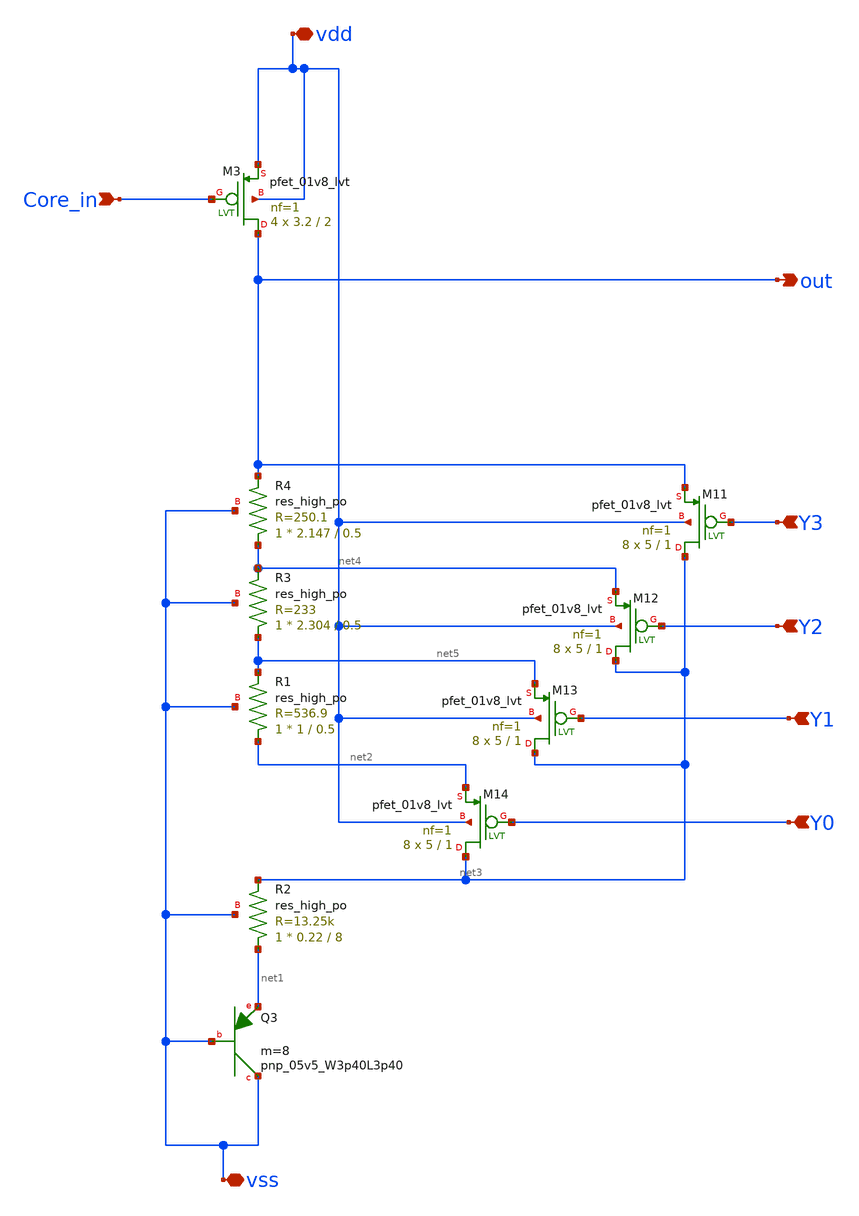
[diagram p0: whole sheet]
** sch_path: Vref_mirror.sch
**.subckt Vref_mirror out vdd vss Core_in Y3 Y2 Y1 Y0
*.opin out
*.iopin vdd
*.iopin vss
*.ipin Core_in
*.ipin Y3
*.ipin Y2
*.ipin Y1
*.ipin Y0
XM3 out Core_in vdd vdd sky130_fd_pr__pfet_01v8_lvt L=2 W=3.2 nf=1 ad='int((1 + 1)/2) * 3.2 / 1 * 0.29'
+ as='int((1 + 2)/2) * 3.2 / 1 * 0.29' pd='2*int((1 + 1)/2) * (3.2 / 1 + 0.29)' ps='2*int((1 + 2)/2) * (3.2 / 1 + 0.29)'
+ nrd='0.29 / 3.2 ' nrs='0.29 / 3.2 ' sa=0 sb=0 sd=0 mult=4 m=4
XQ3 vss vss net1 sky130_fd_pr__pnp_05v5_W3p40L3p40 m=8
XR2 net1 net3 vss sky130_fd_pr__res_high_po W=0.22 L=8 mult=1 m=1
XM11 net3 Y3 out vdd sky130_fd_pr__pfet_01v8_lvt L=1 W=5 nf=1 ad='int((1 + 1)/2) * 5 / 1 * 0.29' as='int((1 + 2)/2) * 5 / 1 * 0.29'
+ pd='2*int((1 + 1)/2) * (5 / 1 + 0.29)' ps='2*int((1 + 2)/2) * (5 / 1 + 0.29)' nrd='0.29 / 5 ' nrs='0.29 / 5 '
+ sa=0 sb=0 sd=0 mult=8 m=8
XM12 net3 Y2 net4 vdd sky130_fd_pr__pfet_01v8_lvt L=1 W=5 nf=1 ad='int((1 + 1)/2) * 5 / 1 * 0.29' as='int((1 + 2)/2) * 5 / 1 * 0.29'
+ pd='2*int((1 + 1)/2) * (5 / 1 + 0.29)' ps='2*int((1 + 2)/2) * (5 / 1 + 0.29)' nrd='0.29 / 5 ' nrs='0.29 / 5 '
+ sa=0 sb=0 sd=0 mult=8 m=8
XM13 net3 Y1 net5 vdd sky130_fd_pr__pfet_01v8_lvt L=1 W=5 nf=1 ad='int((1 + 1)/2) * 5 / 1 * 0.29' as='int((1 + 2)/2) * 5 / 1 * 0.29'
+ pd='2*int((1 + 1)/2) * (5 / 1 + 0.29)' ps='2*int((1 + 2)/2) * (5 / 1 + 0.29)' nrd='0.29 / 5 ' nrs='0.29 / 5 '
+ sa=0 sb=0 sd=0 mult=8 m=8
XM14 net3 Y0 net2 vdd sky130_fd_pr__pfet_01v8_lvt L=1 W=5 nf=1 ad='int((1 + 1)/2) * 5 / 1 * 0.29' as='int((1 + 2)/2) * 5 / 1 * 0.29'
+ pd='2*int((1 + 1)/2) * (5 / 1 + 0.29)' ps='2*int((1 + 2)/2) * (5 / 1 + 0.29)' nrd='0.29 / 5 ' nrs='0.29 / 5 '
+ sa=0 sb=0 sd=0 mult=8 m=8
XR1 net2 net5 vss sky130_fd_pr__res_high_po W=1 L=0.5 mult=1 m=1
XR3 net5 net4 vss sky130_fd_pr__res_high_po W=2.304 L=0.5 mult=1 m=1
XR4 net4 out vss sky130_fd_pr__res_high_po W=2.147 L=0.5 mult=1 m=1
**.ends
.end
